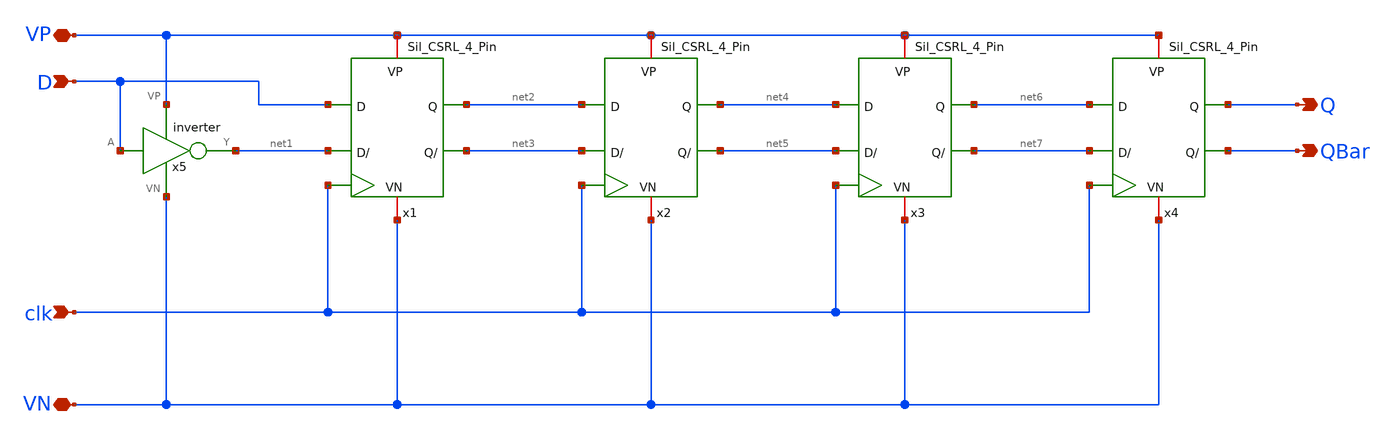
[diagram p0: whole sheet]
** sch_path: MADVLSI_MP2/ShiftReg_xschem_LVS.sch
**.subckt ShiftReg_xschem_LVS D clk VN VP QBar Q
*.ipin D
*.ipin clk
*.iopin VN
*.iopin VP
*.opin QBar
*.opin Q
x5 VP D net1 VN inverter
x1 VP D net2 net3 net1 clk VN Sil_CSRL_4_Pin
x2 VP net2 net4 net5 net3 clk VN Sil_CSRL_4_Pin
x3 VP net4 net6 net7 net5 clk VN Sil_CSRL_4_Pin
x4 VP net6 Q QBar net7 clk VN Sil_CSRL_4_Pin
**.ends

* expanding   symbol:  /home/allan/Documents/MADVLSI_Projects/MADVLSI_MP1/inverter.sym # of pins=4
** sym_path: MADVLSI_MP1/inverter.sym
** sch_path: MADVLSI_MP1/inverter.sch
.subckt inverter VP A Y VN
*.ipin A
*.iopin VP
*.iopin VN
*.opin Y
XM1 Y A VN VN sky130_fd_pr__nfet_01v8 L=0.15 W=1 nf=1 ad='int((nf+1)/2) * W/nf * 0.29' as='int((nf+2)/2) * W/nf * 0.29'
+ pd='2*int((nf+1)/2) * (W/nf + 0.29)' ps='2*int((nf+2)/2) * (W/nf + 0.29)' nrd='0.29 / W' nrs='0.29 / W'
+ sa=0 sb=0 sd=0 mult=1 m=1
XM2 Y A VP VP sky130_fd_pr__pfet_01v8 L=0.15 W=1 nf=1 ad='int((nf+1)/2) * W/nf * 0.29' as='int((nf+2)/2) * W/nf * 0.29'
+ pd='2*int((nf+1)/2) * (W/nf + 0.29)' ps='2*int((nf+2)/2) * (W/nf + 0.29)' nrd='0.29 / W' nrs='0.29 / W'
+ sa=0 sb=0 sd=0 mult=1 m=1
.ends


* expanding   symbol:  Sil_CSRL_4_Pin.sym # of pins=7
** sym_path: MADVLSI_MP2/Sil_CSRL_4_Pin.sym
** sch_path: MADVLSI_MP2/Sil_CSRL_4_Pin.sch
.subckt Sil_CSRL_4_Pin VP D Q QBar DBar clk VN
*.iopin VN
*.iopin VP
*.ipin D
*.ipin DBar
*.ipin clk
*.opin Q
*.opin QBar
XQ1 net1 clk D VP sky130_fd_pr__pfet_01v8 L=0.15 W=0.9 nf=1 ad='int((nf+1)/2) * W/nf * 0.29' as='int((nf+2)/2) * W/nf * 0.29'
+ pd='2*int((nf+1)/2) * (W/nf + 0.29)' ps='2*int((nf+2)/2) * (W/nf + 0.29)' nrd='0.29 / W' nrs='0.29 / W'
+ sa=0 sb=0 sd=0 mult=1 m=1
XQ3 Q clk net1 VN sky130_fd_pr__nfet_01v8 L=0.15 W=0.9 nf=1 ad='int((nf+1)/2) * W/nf * 0.29' as='int((nf+2)/2) * W/nf * 0.29'
+ pd='2*int((nf+1)/2) * (W/nf + 0.29)' ps='2*int((nf+2)/2) * (W/nf + 0.29)' nrd='0.29 / W' nrs='0.29 / W'
+ sa=0 sb=0 sd=0 mult=1 m=1
XQ2 net2 clk DBar VP sky130_fd_pr__pfet_01v8 L=0.15 W=0.9 nf=1 ad='int((nf+1)/2) * W/nf * 0.29' as='int((nf+2)/2) * W/nf * 0.29'
+ pd='2*int((nf+1)/2) * (W/nf + 0.29)' ps='2*int((nf+2)/2) * (W/nf + 0.29)' nrd='0.29 / W' nrs='0.29 / W'
+ sa=0 sb=0 sd=0 mult=1 m=1
XQ8 net2 net1 VP VP sky130_fd_pr__pfet_01v8 L=0.15 W=0.9 nf=1 ad='int((nf+1)/2) * W/nf * 0.29' as='int((nf+2)/2) * W/nf * 0.29'
+ pd='2*int((nf+1)/2) * (W/nf + 0.29)' ps='2*int((nf+2)/2) * (W/nf + 0.29)' nrd='0.29 / W' nrs='0.29 / W'
+ sa=0 sb=0 sd=0 mult=1 m=1
XQ9 VP net2 net1 VP sky130_fd_pr__pfet_01v8 L=0.15 W=0.9 nf=1 ad='int((nf+1)/2) * W/nf * 0.29' as='int((nf+2)/2) * W/nf * 0.29'
+ pd='2*int((nf+1)/2) * (W/nf + 0.29)' ps='2*int((nf+2)/2) * (W/nf + 0.29)' nrd='0.29 / W' nrs='0.29 / W'
+ sa=0 sb=0 sd=0 mult=1 m=1
XQ12 net4 QBar Q VP sky130_fd_pr__pfet_01v8 L=0.15 W=0.9 nf=1 ad='int((nf+1)/2) * W/nf * 0.29' as='int((nf+2)/2) * W/nf * 0.29'
+ pd='2*int((nf+1)/2) * (W/nf + 0.29)' ps='2*int((nf+2)/2) * (W/nf + 0.29)' nrd='0.29 / W' nrs='0.29 / W'
+ sa=0 sb=0 sd=0 mult=1 m=1
XQ10 net4 clk VP VP sky130_fd_pr__pfet_01v8 L=0.15 W=0.9 nf=1 ad='int((nf+1)/2) * W/nf * 0.29' as='int((nf+2)/2) * W/nf * 0.29'
+ pd='2*int((nf+1)/2) * (W/nf + 0.29)' ps='2*int((nf+2)/2) * (W/nf + 0.29)' nrd='0.29 / W' nrs='0.29 / W'
+ sa=0 sb=0 sd=0 mult=1 m=1
XQ11 QBar Q net4 VP sky130_fd_pr__pfet_01v8 L=0.15 W=0.9 nf=1 ad='int((nf+1)/2) * W/nf * 0.29' as='int((nf+2)/2) * W/nf * 0.29'
+ pd='2*int((nf+1)/2) * (W/nf + 0.29)' ps='2*int((nf+2)/2) * (W/nf + 0.29)' nrd='0.29 / W' nrs='0.29 / W'
+ sa=0 sb=0 sd=0 mult=1 m=1
XQ4 QBar clk net2 VN sky130_fd_pr__nfet_01v8 L=0.15 W=0.9 nf=1 ad='int((nf+1)/2) * W/nf * 0.29' as='int((nf+2)/2) * W/nf * 0.29'
+ pd='2*int((nf+1)/2) * (W/nf + 0.29)' ps='2*int((nf+2)/2) * (W/nf + 0.29)' nrd='0.29 / W' nrs='0.29 / W'
+ sa=0 sb=0 sd=0 mult=1 m=1
XQ5a net3 clk VN VN sky130_fd_pr__nfet_01v8 L=0.15 W=0.45 nf=1 ad='int((nf+1)/2) * W/nf * 0.29' as='int((nf+2)/2) * W/nf * 0.29'
+ pd='2*int((nf+1)/2) * (W/nf + 0.29)' ps='2*int((nf+2)/2) * (W/nf + 0.29)' nrd='0.29 / W' nrs='0.29 / W'
+ sa=0 sb=0 sd=0 mult=1 m=1
XQ7 net3 net2 net1 VN sky130_fd_pr__nfet_01v8 L=0.15 W=0.45 nf=1 ad='int((nf+1)/2) * W/nf * 0.29' as='int((nf+2)/2) * W/nf * 0.29'
+ pd='2*int((nf+1)/2) * (W/nf + 0.29)' ps='2*int((nf+2)/2) * (W/nf + 0.29)' nrd='0.29 / W' nrs='0.29 / W'
+ sa=0 sb=0 sd=0 mult=1 m=1
XQ6 net2 net1 net3 VN sky130_fd_pr__nfet_01v8 L=0.15 W=0.45 nf=1 ad='int((nf+1)/2) * W/nf * 0.29' as='int((nf+2)/2) * W/nf * 0.29'
+ pd='2*int((nf+1)/2) * (W/nf + 0.29)' ps='2*int((nf+2)/2) * (W/nf + 0.29)' nrd='0.29 / W' nrs='0.29 / W'
+ sa=0 sb=0 sd=0 mult=1 m=1
XQ13 QBar Q VN VN sky130_fd_pr__nfet_01v8 L=0.15 W=0.45 nf=1 ad='int((nf+1)/2) * W/nf * 0.29' as='int((nf+2)/2) * W/nf * 0.29'
+ pd='2*int((nf+1)/2) * (W/nf + 0.29)' ps='2*int((nf+2)/2) * (W/nf + 0.29)' nrd='0.29 / W' nrs='0.29 / W'
+ sa=0 sb=0 sd=0 mult=1 m=1
XQ14 VN QBar Q VN sky130_fd_pr__nfet_01v8 L=0.15 W=0.45 nf=1 ad='int((nf+1)/2) * W/nf * 0.29' as='int((nf+2)/2) * W/nf * 0.29'
+ pd='2*int((nf+1)/2) * (W/nf + 0.29)' ps='2*int((nf+2)/2) * (W/nf + 0.29)' nrd='0.29 / W' nrs='0.29 / W'
+ sa=0 sb=0 sd=0 mult=1 m=1
XQ5b VN clk net3 VN sky130_fd_pr__nfet_01v8 L=0.15 W=0.45 nf=1 ad='int((nf+1)/2) * W/nf * 0.29' as='int((nf+2)/2) * W/nf * 0.29'
+ pd='2*int((nf+1)/2) * (W/nf + 0.29)' ps='2*int((nf+2)/2) * (W/nf + 0.29)' nrd='0.29 / W' nrs='0.29 / W'
+ sa=0 sb=0 sd=0 mult=1 m=1
XQ10b VP clk net4 VP sky130_fd_pr__pfet_01v8 L=0.15 W=0.9 nf=1 ad='int((nf+1)/2) * W/nf * 0.29' as='int((nf+2)/2) * W/nf * 0.29'
+ pd='2*int((nf+1)/2) * (W/nf + 0.29)' ps='2*int((nf+2)/2) * (W/nf + 0.29)' nrd='0.29 / W' nrs='0.29 / W'
+ sa=0 sb=0 sd=0 mult=1 m=1
.ends

.end
